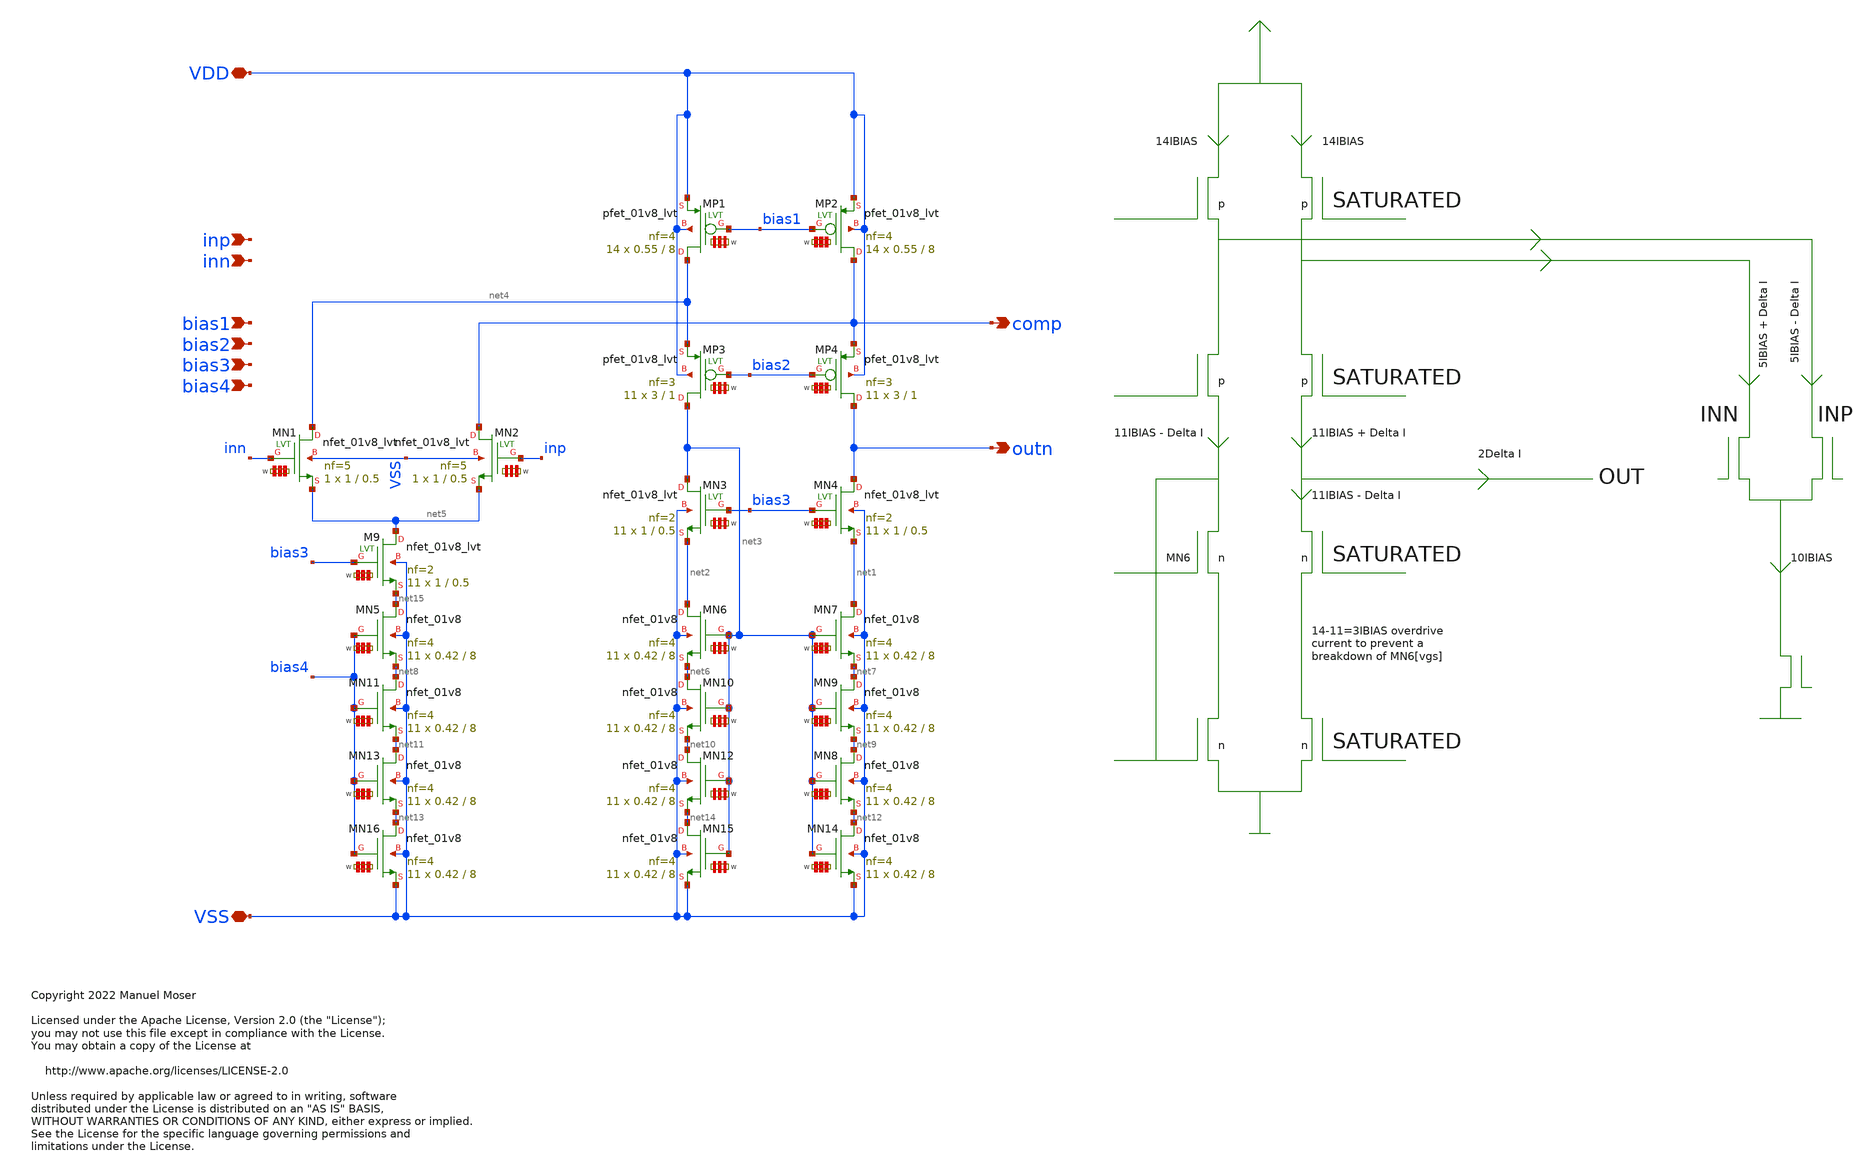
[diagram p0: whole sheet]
** sch_path: xschem/ldo_fc_n.sch
* Copyright 2022 Manuel Moser
* Licensed under the Apache License, Version 2.0 (the "License");
**.subckt ldo_fc_n VSS VDD inp inn bias1 outn bias2 bias3 bias4 comp
*.iopin VSS
*.iopin VDD
*.ipin inp
*.ipin inn
*.ipin bias1
*.opin outn
*.ipin bias2
*.ipin bias3
*.ipin bias4
*.opin comp
XMN4 outn bias3 net1 VSS sky130_fd_pr__nfet_01v8_lvt L=0.5 W='1 * 2 ' nf=2 ad='int((nf+1)/2) * W / nf * 0.29'
+ as='int((nf+2)/2) * W / nf * 0.29' pd='2*int((nf+1)/2) * (W / nf + 0.29)' ps='2*int((nf+2)/2) * (W / nf + 0.29)'
+ nrd='0.29 / W ' nrs='0.29 / W ' sa=0 sb=0 sd=0 mult=11 m=11
XMN7 net1 net3 net7 VSS sky130_fd_pr__nfet_01v8 L=8 W='0.42 * 4 ' nf=4 ad='int((nf+1)/2) * W / nf * 0.29'
+ as='int((nf+2)/2) * W / nf * 0.29' pd='2*int((nf+1)/2) * (W / nf + 0.29)' ps='2*int((nf+2)/2) * (W / nf + 0.29)'
+ nrd='0.29 / W ' nrs='0.29 / W ' sa=0 sb=0 sd=0 mult=11 m=11
XMN3 net3 bias3 net2 VSS sky130_fd_pr__nfet_01v8_lvt L=0.5 W='1 * 2 ' nf=2 ad='int((nf+1)/2) * W / nf * 0.29'
+ as='int((nf+2)/2) * W / nf * 0.29' pd='2*int((nf+1)/2) * (W / nf + 0.29)' ps='2*int((nf+2)/2) * (W / nf + 0.29)'
+ nrd='0.29 / W ' nrs='0.29 / W ' sa=0 sb=0 sd=0 mult=11 m=11
XMN6 net2 net3 net6 VSS sky130_fd_pr__nfet_01v8 L=8 W='0.42 * 4 ' nf=4 ad='int((nf+1)/2) * W / nf * 0.29'
+ as='int((nf+2)/2) * W / nf * 0.29' pd='2*int((nf+1)/2) * (W / nf + 0.29)' ps='2*int((nf+2)/2) * (W / nf + 0.29)'
+ nrd='0.29 / W ' nrs='0.29 / W ' sa=0 sb=0 sd=0 mult=11 m=11
XMP4 outn bias2 comp VDD sky130_fd_pr__pfet_01v8_lvt L=1 W='3 * 3 ' nf=3 ad='int((nf+1)/2) * W / nf * 0.29'
+ as='int((nf+2)/2) * W / nf * 0.29' pd='2*int((nf+1)/2) * (W / nf + 0.29)' ps='2*int((nf+2)/2) * (W / nf + 0.29)'
+ nrd='0.29 / W ' nrs='0.29 / W ' sa=0 sb=0 sd=0 mult=11 m=11
XMP2 comp bias1 VDD VDD sky130_fd_pr__pfet_01v8_lvt L=8 W='0.55 * 4 ' nf=4 ad='int((nf+1)/2) * W / nf * 0.29'
+ as='int((nf+2)/2) * W / nf * 0.29' pd='2*int((nf+1)/2) * (W / nf + 0.29)' ps='2*int((nf+2)/2) * (W / nf + 0.29)'
+ nrd='0.29 / W ' nrs='0.29 / W ' sa=0 sb=0 sd=0 mult=14 m=14
XMP3 net3 bias2 net4 VDD sky130_fd_pr__pfet_01v8_lvt L=1 W='3 * 3 ' nf=3 ad='int((nf+1)/2) * W / nf * 0.29'
+ as='int((nf+2)/2) * W / nf * 0.29' pd='2*int((nf+1)/2) * (W / nf + 0.29)' ps='2*int((nf+2)/2) * (W / nf + 0.29)'
+ nrd='0.29 / W ' nrs='0.29 / W ' sa=0 sb=0 sd=0 mult=11 m=11
XMP1 net4 bias1 VDD VDD sky130_fd_pr__pfet_01v8_lvt L=8 W='0.55 * 4 ' nf=4 ad='int((nf+1)/2) * W / nf * 0.29'
+ as='int((nf+2)/2) * W / nf * 0.29' pd='2*int((nf+1)/2) * (W / nf + 0.29)' ps='2*int((nf+2)/2) * (W / nf + 0.29)'
+ nrd='0.29 / W ' nrs='0.29 / W ' sa=0 sb=0 sd=0 mult=14 m=14
XMN5 net15 bias4 net8 VSS sky130_fd_pr__nfet_01v8 L=8 W='0.42 * 4 ' nf=4 ad='int((nf+1)/2) * W / nf * 0.29'
+ as='int((nf+2)/2) * W / nf * 0.29' pd='2*int((nf+1)/2) * (W / nf + 0.29)' ps='2*int((nf+2)/2) * (W / nf + 0.29)'
+ nrd='0.29 / W ' nrs='0.29 / W ' sa=0 sb=0 sd=0 mult=11 m=11
XMN1 net4 inn net5 VSS sky130_fd_pr__nfet_01v8_lvt L=0.5 W='1 * 5 ' nf=5 ad='int((nf+1)/2) * W / nf * 0.29'
+ as='int((nf+2)/2) * W / nf * 0.29' pd='2*int((nf+1)/2) * (W / nf + 0.29)' ps='2*int((nf+2)/2) * (W / nf + 0.29)'
+ nrd='0.29 / W ' nrs='0.29 / W ' sa=0 sb=0 sd=0 mult=1 m=1
XMN2 comp inp net5 VSS sky130_fd_pr__nfet_01v8_lvt L=0.5 W='1 * 5 ' nf=5 ad='int((nf+1)/2) * W / nf * 0.29'
+ as='int((nf+2)/2) * W / nf * 0.29' pd='2*int((nf+1)/2) * (W / nf + 0.29)' ps='2*int((nf+2)/2) * (W / nf + 0.29)'
+ nrd='0.29 / W ' nrs='0.29 / W ' sa=0 sb=0 sd=0 mult=1 m=1
XMN9 net7 net3 net9 VSS sky130_fd_pr__nfet_01v8 L=8 W='0.42 * 4 ' nf=4 ad='int((nf+1)/2) * W / nf * 0.29'
+ as='int((nf+2)/2) * W / nf * 0.29' pd='2*int((nf+1)/2) * (W / nf + 0.29)' ps='2*int((nf+2)/2) * (W / nf + 0.29)'
+ nrd='0.29 / W ' nrs='0.29 / W ' sa=0 sb=0 sd=0 mult=11 m=11
XMN10 net6 net3 net10 VSS sky130_fd_pr__nfet_01v8 L=8 W='0.42 * 4 ' nf=4 ad='int((nf+1)/2) * W / nf * 0.29'
+ as='int((nf+2)/2) * W / nf * 0.29' pd='2*int((nf+1)/2) * (W / nf + 0.29)' ps='2*int((nf+2)/2) * (W / nf + 0.29)'
+ nrd='0.29 / W ' nrs='0.29 / W ' sa=0 sb=0 sd=0 mult=11 m=11
XMN11 net8 bias4 net11 VSS sky130_fd_pr__nfet_01v8 L=8 W='0.42 * 4 ' nf=4 ad='int((nf+1)/2) * W / nf * 0.29'
+ as='int((nf+2)/2) * W / nf * 0.29' pd='2*int((nf+1)/2) * (W / nf + 0.29)' ps='2*int((nf+2)/2) * (W / nf + 0.29)'
+ nrd='0.29 / W ' nrs='0.29 / W ' sa=0 sb=0 sd=0 mult=11 m=11
XMN8 net9 net3 net12 VSS sky130_fd_pr__nfet_01v8 L=8 W='0.42 * 4 ' nf=4 ad='int((nf+1)/2) * W / nf * 0.29'
+ as='int((nf+2)/2) * W / nf * 0.29' pd='2*int((nf+1)/2) * (W / nf + 0.29)' ps='2*int((nf+2)/2) * (W / nf + 0.29)'
+ nrd='0.29 / W ' nrs='0.29 / W ' sa=0 sb=0 sd=0 mult=11 m=11
XMN12 net10 net3 net14 VSS sky130_fd_pr__nfet_01v8 L=8 W='0.42 * 4 ' nf=4 ad='int((nf+1)/2) * W / nf * 0.29'
+ as='int((nf+2)/2) * W / nf * 0.29' pd='2*int((nf+1)/2) * (W / nf + 0.29)' ps='2*int((nf+2)/2) * (W / nf + 0.29)'
+ nrd='0.29 / W ' nrs='0.29 / W ' sa=0 sb=0 sd=0 mult=11 m=11
XMN13 net11 bias4 net13 VSS sky130_fd_pr__nfet_01v8 L=8 W='0.42 * 4 ' nf=4 ad='int((nf+1)/2) * W / nf * 0.29'
+ as='int((nf+2)/2) * W / nf * 0.29' pd='2*int((nf+1)/2) * (W / nf + 0.29)' ps='2*int((nf+2)/2) * (W / nf + 0.29)'
+ nrd='0.29 / W ' nrs='0.29 / W ' sa=0 sb=0 sd=0 mult=11 m=11
XMN14 net12 net3 VSS VSS sky130_fd_pr__nfet_01v8 L=8 W='0.42 * 4 ' nf=4 ad='int((nf+1)/2) * W / nf * 0.29'
+ as='int((nf+2)/2) * W / nf * 0.29' pd='2*int((nf+1)/2) * (W / nf + 0.29)' ps='2*int((nf+2)/2) * (W / nf + 0.29)'
+ nrd='0.29 / W ' nrs='0.29 / W ' sa=0 sb=0 sd=0 mult=11 m=11
XMN15 net14 net3 VSS VSS sky130_fd_pr__nfet_01v8 L=8 W='0.42 * 4 ' nf=4 ad='int((nf+1)/2) * W / nf * 0.29'
+ as='int((nf+2)/2) * W / nf * 0.29' pd='2*int((nf+1)/2) * (W / nf + 0.29)' ps='2*int((nf+2)/2) * (W / nf + 0.29)'
+ nrd='0.29 / W ' nrs='0.29 / W ' sa=0 sb=0 sd=0 mult=11 m=11
XMN16 net13 bias4 VSS VSS sky130_fd_pr__nfet_01v8 L=8 W='0.42 * 4 ' nf=4 ad='int((nf+1)/2) * W / nf * 0.29'
+ as='int((nf+2)/2) * W / nf * 0.29' pd='2*int((nf+1)/2) * (W / nf + 0.29)' ps='2*int((nf+2)/2) * (W / nf + 0.29)'
+ nrd='0.29 / W ' nrs='0.29 / W ' sa=0 sb=0 sd=0 mult=11 m=11
XM9 net5 bias3 net15 VSS sky130_fd_pr__nfet_01v8_lvt L=0.5 W='1 * 2 ' nf=2 ad='int((nf+1)/2) * W / nf * 0.29'
+ as='int((nf+2)/2) * W / nf * 0.29' pd='2*int((nf+1)/2) * (W / nf + 0.29)' ps='2*int((nf+2)/2) * (W / nf + 0.29)'
+ nrd='0.29 / W ' nrs='0.29 / W ' sa=0 sb=0 sd=0 mult=11 m=11
**.ends
.end
